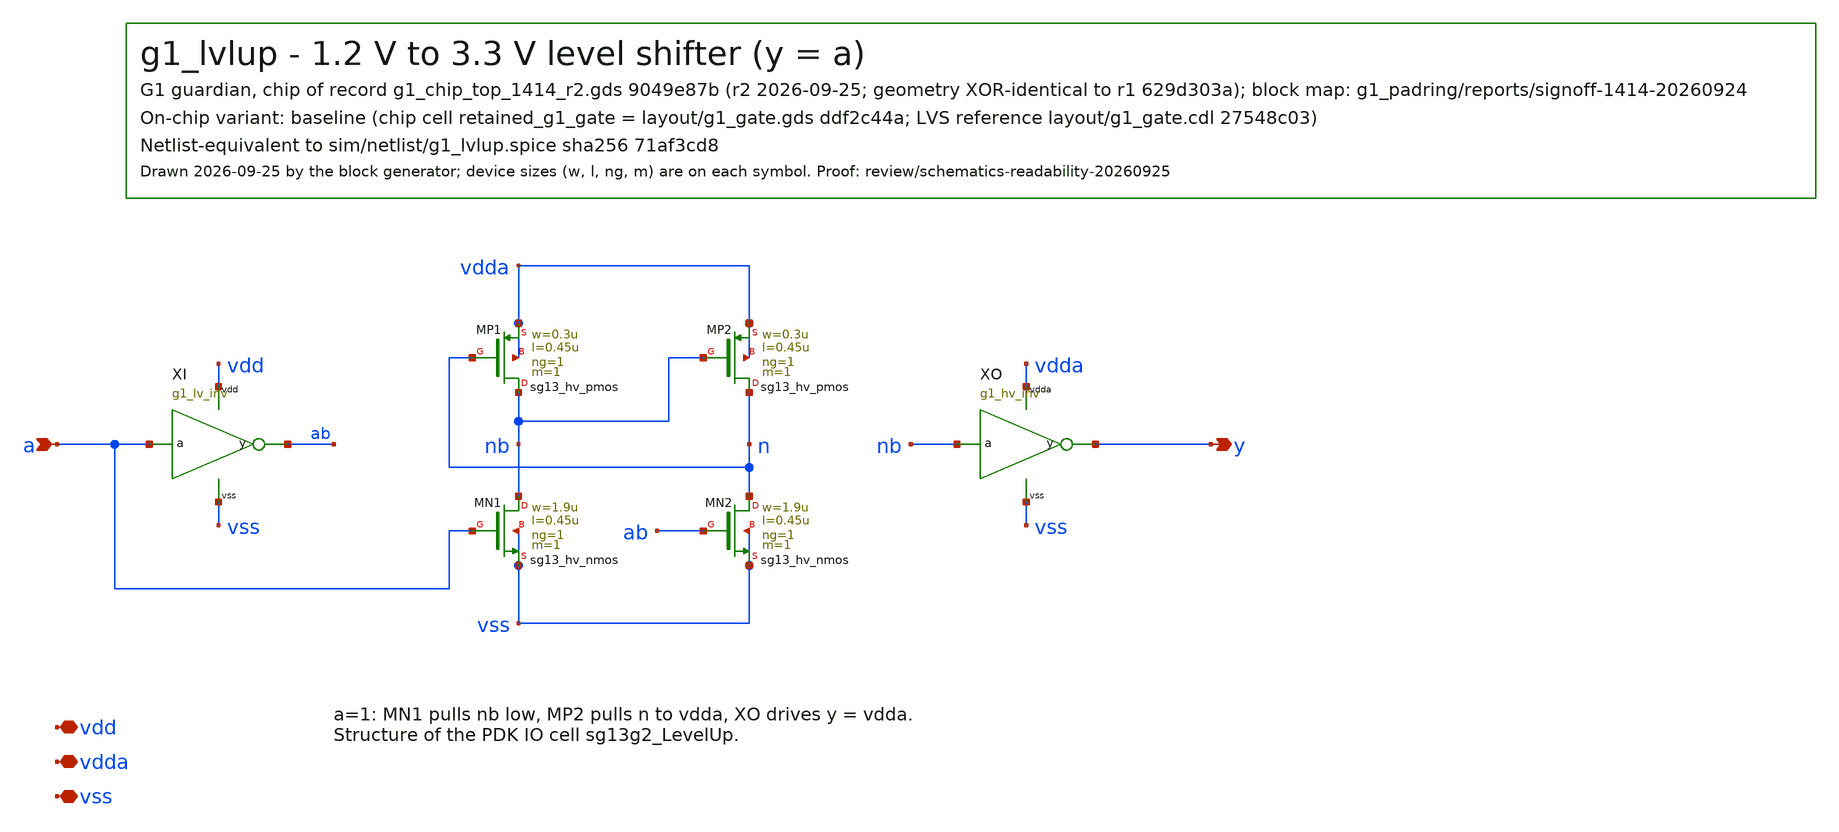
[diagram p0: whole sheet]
** sch_path: designs/g1-guardian/blocks/g1_gate/schematic/g1_lvlup.sch
**.subckt g1_lvlup a y vdd vdda vss
*.ipin a
*.opin y
*.iopin vdd
*.iopin vdda
*.iopin vss
XI a ab vdd vss g1_lv_inv
XMN1 nb a vss vss sg13_hv_nmos w=1.9u l=0.45u ng=1 m=1 mm_ok=1
XMN2 n ab vss vss sg13_hv_nmos w=1.9u l=0.45u ng=1 m=1 mm_ok=1
XMP1 nb n vdda vdda sg13_hv_pmos w=0.3u l=0.45u ng=1 m=1 mm_ok=1
XMP2 n nb vdda vdda sg13_hv_pmos w=0.3u l=0.45u ng=1 m=1 mm_ok=1
XO nb y vdda vss g1_hv_inv
**.ends

* expanding   symbol:  g1_lv_inv.sym # of pins=4
** sym_path: designs/g1-guardian/blocks/g1_gate/schematic/g1_lv_inv.sym
** sch_path: designs/g1-guardian/blocks/g1_gate/schematic/g1_lv_inv.sch
.subckt g1_lv_inv a y vdd vss
*.ipin a
*.opin y
*.iopin vdd
*.iopin vss
XMP y a vdd vdd sg13_lv_pmos w=2u l=0.13u ng=1 m=1 mm_ok=1
XMN y a vss vss sg13_lv_nmos w=1u l=0.13u ng=1 m=1 mm_ok=1
.ends


* expanding   symbol:  g1_hv_inv.sym # of pins=4
** sym_path: designs/g1-guardian/blocks/g1_gate/schematic/g1_hv_inv.sym
** sch_path: designs/g1-guardian/blocks/g1_gate/schematic/g1_hv_inv.sch
.subckt g1_hv_inv a y vdda vss
*.ipin a
*.opin y
*.iopin vdda
*.iopin vss
XMP y a vdda vdda sg13_hv_pmos w=3.9u l=0.45u ng=1 m=1 mm_ok=1
XMN y a vss vss sg13_hv_nmos w=1.9u l=0.45u ng=1 m=1 mm_ok=1
.ends

.end
